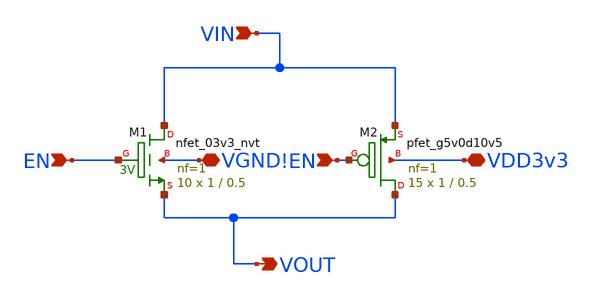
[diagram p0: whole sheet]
** sch_path: xschem/analogue_switch.sch
**.subckt analogue_switch VGND VDD3v3 EN VIN !EN VOUT
*.iopin VGND
*.iopin VDD3v3
*.ipin EN
*.ipin VIN
*.ipin !EN
*.opin VOUT
XM2 VOUT !EN VIN VDD3v3 sky130_fd_pr__pfet_g5v0d10v5 L=0.5 W=1 nf=1 ad='int((nf+1)/2) * W/nf * 0.29'
+ as='int((nf+2)/2) * W/nf * 0.29' pd='2*int((nf+1)/2) * (W/nf + 0.29)' ps='2*int((nf+2)/2) * (W/nf + 0.29)'
+ nrd='0.29 / W' nrs='0.29 / W' sa=0 sb=0 sd=0 mult=15 m=15
XM1 VIN EN VOUT VGND sky130_fd_pr__nfet_03v3_nvt L=0.5 W=1 nf=1 ad='int((nf+1)/2) * W/nf * 0.29' as='int((nf+2)/2) * W/nf * 0.29'
+ pd='2*int((nf+1)/2) * (W/nf + 0.29)' ps='2*int((nf+2)/2) * (W/nf + 0.29)' nrd='0.29 / W' nrs='0.29 / W'
+ sa=0 sb=0 sd=0 mult=10 m=10
**.ends
.end
